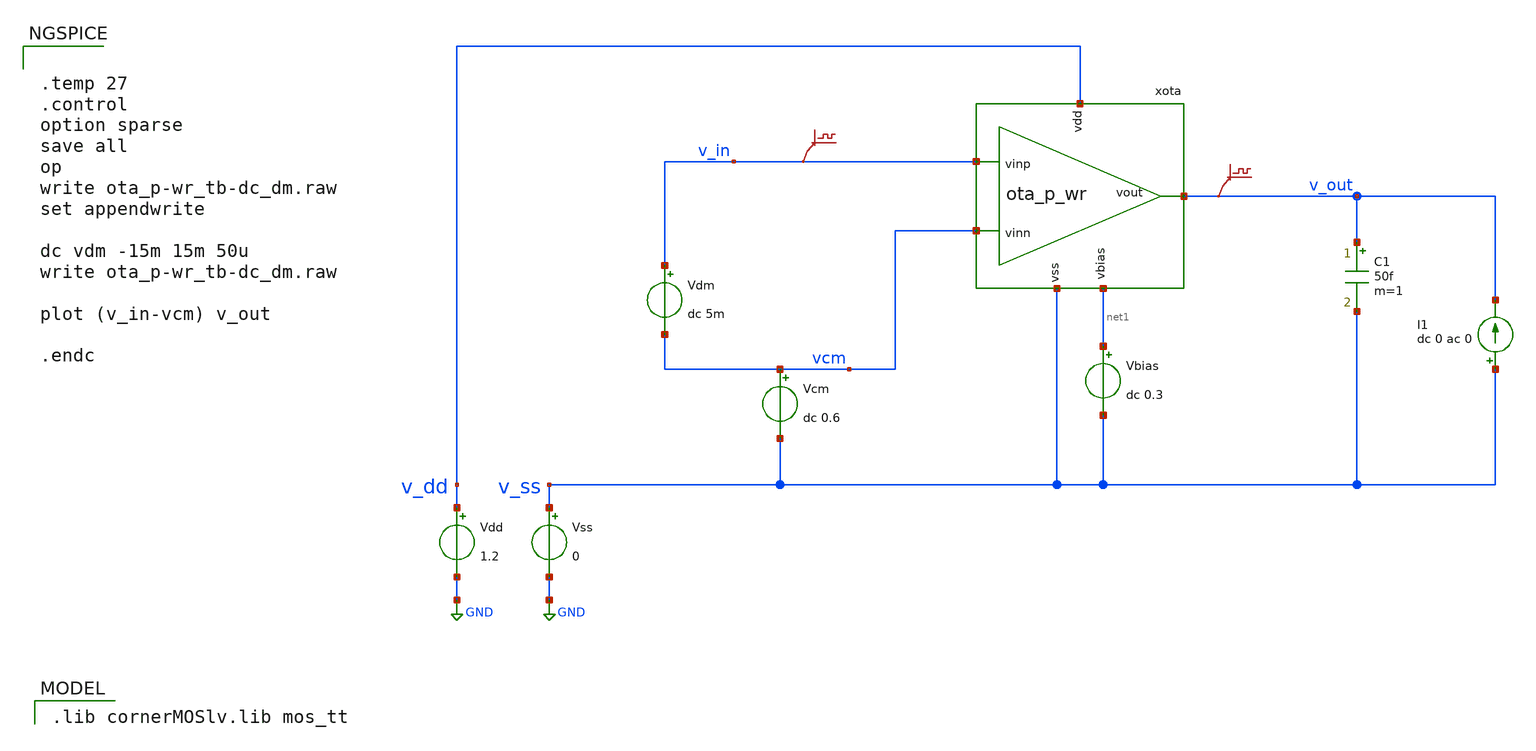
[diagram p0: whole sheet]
** sch_path: v2_feature_extr_withf/ota_p-wr_tb-dc_dm.sch
* (c) 2024-2025 Harald Pretl, Apache-2.0 license
**.subckt ota_p-wr_tb-dc_dm
Vdd v_dd GND 1.2
xota v_dd v_out v_in vcm net1 v_ss ota_p_wr
Vss v_ss GND 0
C1 v_out v_ss 50f m=1
Vcm vcm v_ss dc 0.6
.save v(v_in)
.save v(v_out)
I1 v_ss v_out dc 0 ac 0
Vdm v_in vcm dc 5m
Vbias net1 v_ss dc 0.3
**** begin user architecture code
 .lib cornerMOSlv.lib mos_tt



.temp 27
.control
option sparse
save all
op
write ota_p-wr_tb-dc_dm.raw
set appendwrite

dc vdm -15m 15m 50u
write ota_p-wr_tb-dc_dm.raw

plot (v_in-vcm) v_out

.endc


**** end user architecture code
**.ends
.GLOBAL GND
.end
